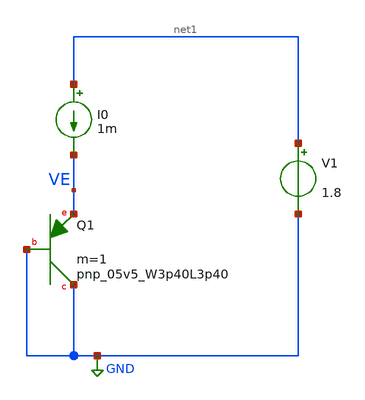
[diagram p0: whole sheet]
** sch_path: design/bgr_new/CTAT.sch
**.subckt CTAT
XQ1 GND GND VE sky130_fd_pr__pnp_05v5_W3p40L3p40 m=1
I0 net1 VE 1m
V1 net1 GND 1.8
**** begin user architecture code

** opencircuitdesign pdks install
.lib $::SKYWATER_MODELS/sky130.lib.spice tt_mm




.options savecurrents

*** plot vbgp with variation in supply voltage
*Vdd VDD GND 3.3
*V_en en GND 3.3
*.dc Vdd 2 4 0.1
*.control
*run
*print Vbgp
*plot V(Vbgp)
*.endc

*** plot vbgp with variation in temperature @3.3V
Vdd VDD GND 3.3
V_en en GND 3.3
.dc temp -40 140 1
.control
run
print V(VE)
plot V(VE)
.endc

*** plot voltage coefficient
*Vdd VDD GND 3.3
*V_en en GND 3.3
*.dc Vdd 2 4 0.1
*.control
*run
*plot deriv(V(Vbgp))
*.endc

*** plot temperature coefficient
*Vdd VDD GND 3.3
*V_en en GND 3.3
*.dc temp -40 140 1
*.control
*run
*plot deriv(V(Vbgp))/1.202344
*.endc



*** enable pin
*Vdd VDD GND 3.3
*V_en en GND PULSE(0 3.3 0 200us 200us 600us 2000us 0)
*.tran 1u 2000us
*.control
*run
*plot V(en)
*plot -I(VDD)
*.endc


**** end user architecture code
**.ends
.GLOBAL GND
.end
